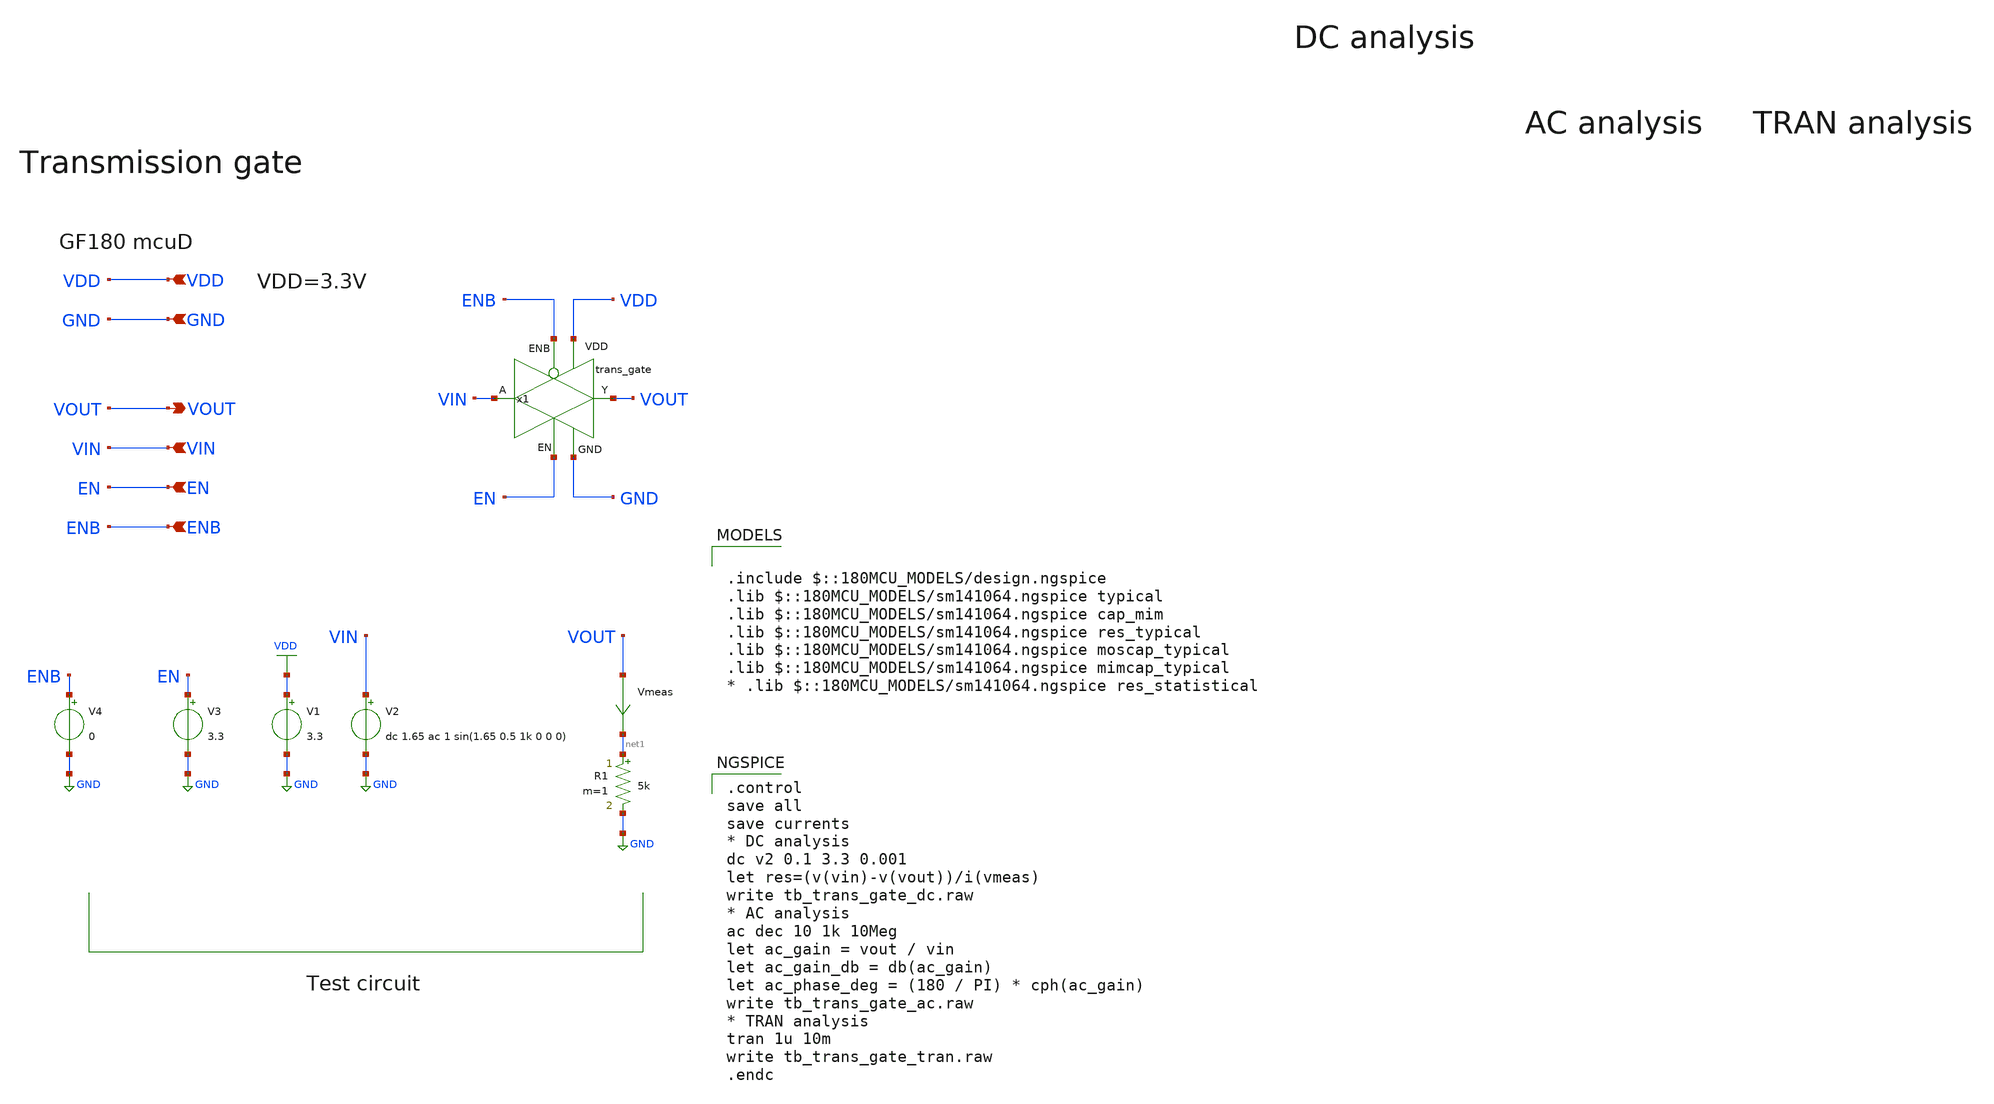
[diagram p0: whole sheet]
** sch_path: designs/libs/tb_analog/tb_trans_gate/tb_trans_gate.sch
* Copyright 2022 GlobalFoundries PDK Authors
* Licensed under the Apache License, Version 2.0 (the "License");
* you may not use this file except in compliance with the License.
* You may obtain a copy of the License at
* https://www.apache.org/licenses/LICENSE-2.0
* Unless required by applicable law or agreed to in writing, software
* distributed under the License is distributed on an "AS IS" BASIS,
* WITHOUT WARRANTIES OR CONDITIONS OF ANY KIND, either express or implied.
* See the License for the specific language governing permissions and
* limitations under the License.
**.subckt tb_trans_gate VDD GND VOUT VIN EN ENB
*.ipin VDD
*.ipin GND
*.opin VOUT
*.ipin VIN
*.ipin EN
*.ipin ENB
V1 VDD GND 3.3
V2 VIN GND dc 1.65 ac 1 sin(1.65 0.5 1k 0 0 0)
Vmeas VOUT net1 0
.save i(vmeas)
R1 net1 GND 5k m=1
V3 EN GND 3.3
V4 ENB GND 0
x1 VDD GND VIN ENB VOUT EN trans_gate
**** begin user architecture code

.control
save all
save currents
* DC analysis
dc v2 0.1 3.3 0.001
let res=(v(vin)-v(vout))/i(vmeas)
write tb_trans_gate_dc.raw
* AC analysis
ac dec 10 1k 10Meg
let ac_gain = vout / vin
let ac_gain_db = db(ac_gain)
let ac_phase_deg = (180 / PI) * cph(ac_gain)
write tb_trans_gate_ac.raw
* TRAN analysis
tran 1u 10m
write tb_trans_gate_tran.raw
.endc



.include $::180MCU_MODELS/design.ngspice
.lib $::180MCU_MODELS/sm141064.ngspice typical
.lib $::180MCU_MODELS/sm141064.ngspice cap_mim
.lib $::180MCU_MODELS/sm141064.ngspice res_typical
.lib $::180MCU_MODELS/sm141064.ngspice moscap_typical
.lib $::180MCU_MODELS/sm141064.ngspice mimcap_typical
* .lib $::180MCU_MODELS/sm141064.ngspice res_statistical

**** end user architecture code
**.ends
.GLOBAL VDD
.GLOBAL GND
.end
